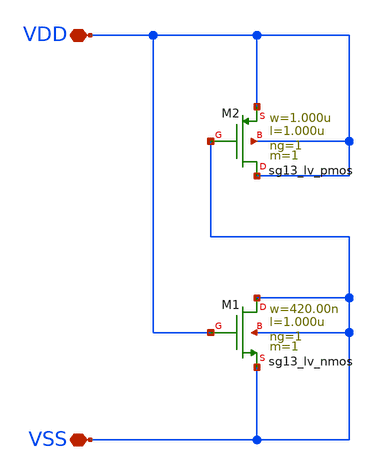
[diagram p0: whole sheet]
** sch_path: ihp-sg13g2/libs.tech/xschem/sg13g2_stdcells/sg13g2_decap_4.sch
**.subckt sg13g2_decap_4 VDD VSS
*.iopin VDD
*.iopin VSS
XM1 VSS VDD VSS VSS sg13_lv_nmos w=420.00n l=1.000u ng=1 m=1 mm_ok=1
XM2 VDD VSS VDD VDD sg13_lv_pmos w=1.000u l=1.000u ng=1 m=1 mm_ok=1
**.ends
.end
